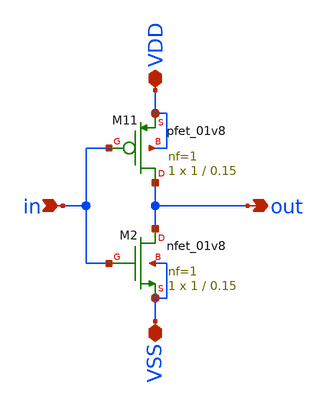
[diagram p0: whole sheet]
** sch_path: xsch/ip/inv/inv.sch
**.subckt inv in out VDD VSS
*.ipin in
*.opin out
*.iopin VDD
*.iopin VSS
XM2 out in VSS VSS sky130_fd_pr__nfet_01v8 L=0.15 W=1 nf=1 ad='int((1 + 1)/2) * 1 / 1 * 0.29' as='int((1 + 2)/2) * 1 / 1 * 0.29'
+ pd='2*int((1 + 1)/2) * (1 / 1 + 0.29)' ps='2*int((1 + 2)/2) * (1 / 1 + 0.29)' nrd='0.29 / 1 ' nrs='0.29 / 1 '
+ sa=0 sb=0 sd=0 mult=1 m=1
XM11 out in VDD VDD sky130_fd_pr__pfet_01v8 L=0.15 W=1 nf=1 ad='int((nf+1)/2) * W/nf * 0.29' as='int((nf+2)/2) * W/nf * 0.29'
+ pd='2*int((nf+1)/2) * (W/nf + 0.29)' ps='2*int((nf+2)/2) * (W/nf + 0.29)' nrd='0.29 / W' nrs='0.29 / W'
+ sa=0 sb=0 sd=0 mult=1 m=1
**.ends
.end
